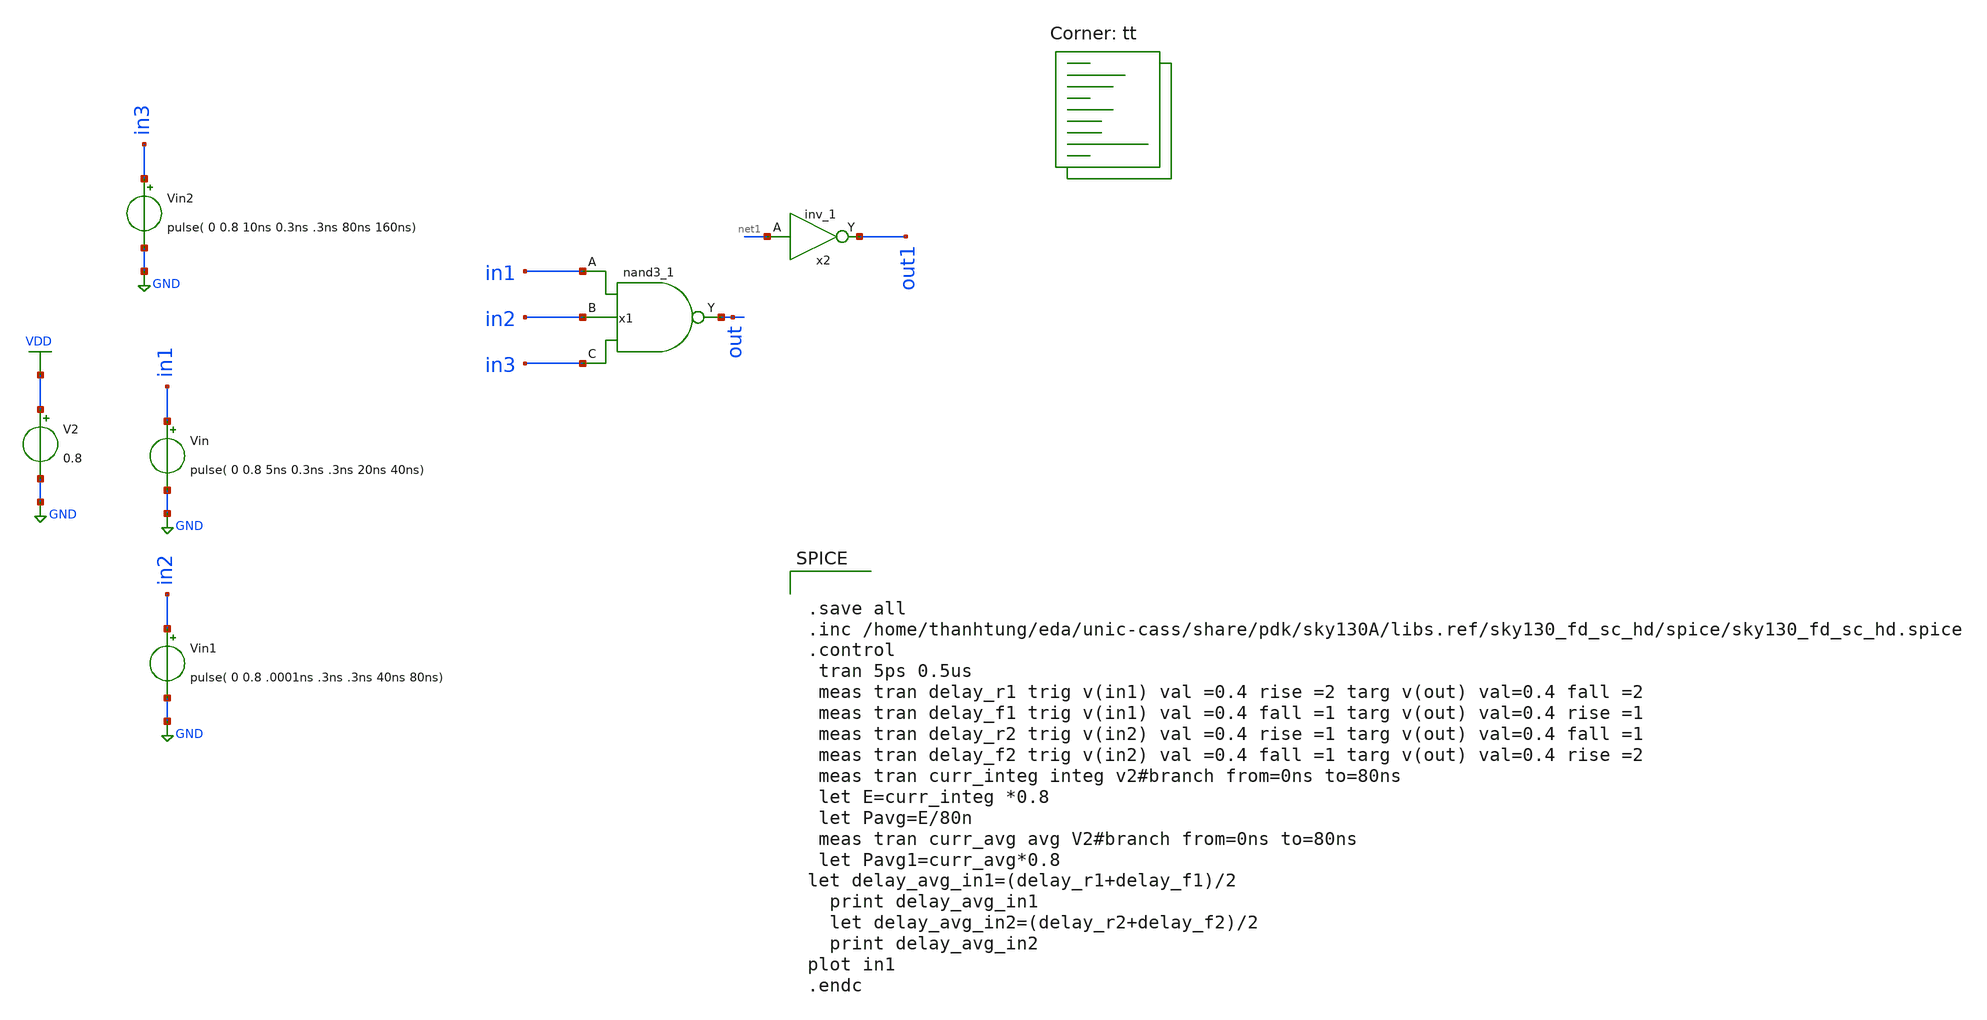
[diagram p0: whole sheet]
** sch_path: d_3nand_para.sch
**.subckt d_3nand_para
V2 VDD GND 0.8
Vin in1 GND pulse( 0 0.8 5ns 0.3ns .3ns 20ns 40ns)
x1 in1 in2 in3 GND GND VDD VDD out sky130_fd_sc_hd__nand3_1
Vin1 in2 GND pulse( 0 0.8 .0001ns .3ns .3ns 40ns 80ns)
Vin2 in3 GND pulse( 0 0.8 10ns 0.3ns .3ns 80ns 160ns)
x2 net1 GND GND VDD VDD out1 sky130_fd_sc_hd__inv_1
**** begin user architecture code


.save all
.inc /home/thanhtung/eda/unic-cass/share/pdk/sky130A/libs.ref/sky130_fd_sc_hd/spice/sky130_fd_sc_hd.spice
.control
 tran 5ps 0.5us
 meas tran delay_r1 trig v(in1) val =0.4 rise =2 targ v(out) val=0.4 fall =2
 meas tran delay_f1 trig v(in1) val =0.4 fall =1 targ v(out) val=0.4 rise =1
 meas tran delay_r2 trig v(in2) val =0.4 rise =1 targ v(out) val=0.4 fall =1
 meas tran delay_f2 trig v(in2) val =0.4 fall =1 targ v(out) val=0.4 rise =2
 meas tran curr_integ integ v2#branch from=0ns to=80ns
 let E=curr_integ *0.8
 let Pavg=E/80n
 meas tran curr_avg avg V2#branch from=0ns to=80ns
 let Pavg1=curr_avg*0.8
let delay_avg_in1=(delay_r1+delay_f1)/2
  print delay_avg_in1
  let delay_avg_in2=(delay_r2+delay_f2)/2
  print delay_avg_in2
plot in1
.endc


.lib $::SKYWATER_MODELS/sky130.lib.spice tt
**** end user architecture code
**.ends
.GLOBAL GND
.GLOBAL VDD
.end
